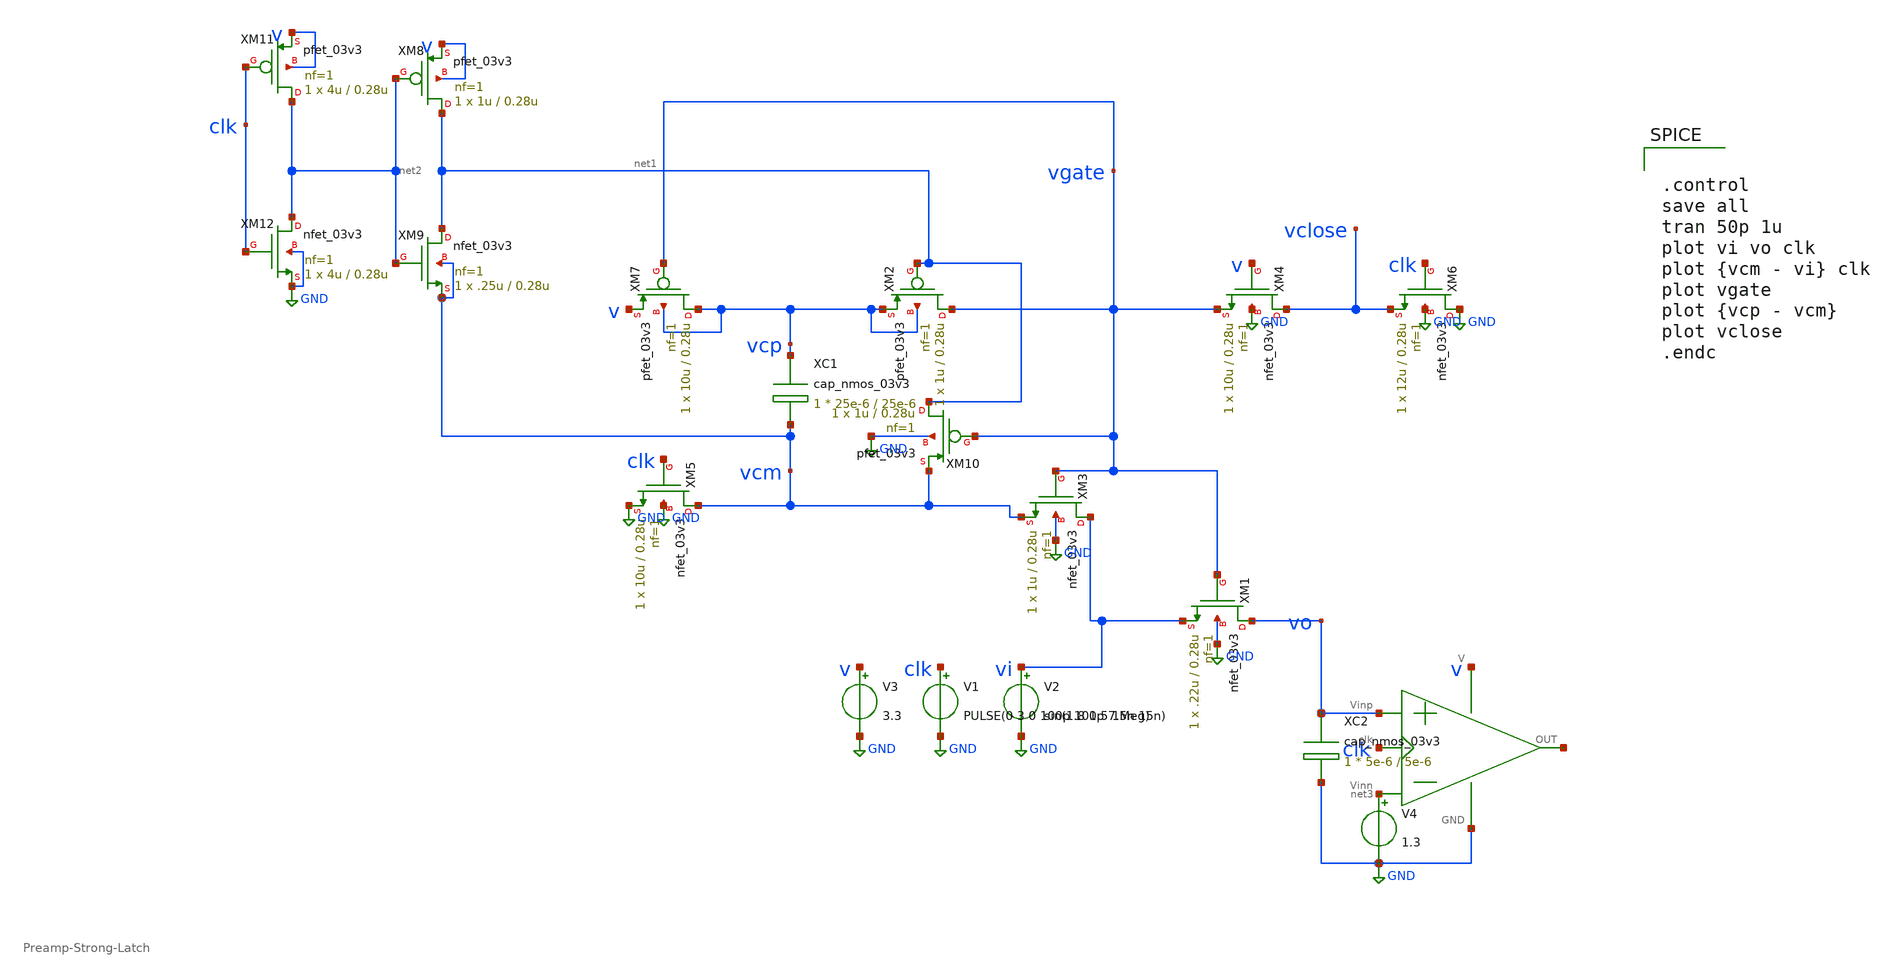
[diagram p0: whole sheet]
** sch_path: btsw/btsw_3.sch
**.subckt btsw_3
XM1 vo vgate vi GND nfet_03v3 L=0.28u W=.22u nf=1 ad='int((nf+1)/2) * W/nf * 0.18u' as='int((nf+2)/2) * W/nf * 0.18u'
+ pd='2*int((nf+1)/2) * (W/nf + 0.18u)' ps='2*int((nf+2)/2) * (W/nf + 0.18u)' nrd='0.18u / W' nrs='0.18u / W'
+ sa=0 sb=0 sd=0 m=1
XM2 vgate net1 vcp vcp pfet_03v3 L=0.28u W=1u nf=1 ad='int((nf+1)/2) * W/nf * 0.18u' as='int((nf+2)/2) * W/nf * 0.18u'
+ pd='2*int((nf+1)/2) * (W/nf + 0.18u)' ps='2*int((nf+2)/2) * (W/nf + 0.18u)' nrd='0.18u / W' nrs='0.18u / W'
+ sa=0 sb=0 sd=0 m=1
XM3 vi vgate vcm GND nfet_03v3 L=0.28u W=1u nf=1 ad='int((nf+1)/2) * W/nf * 0.18u' as='int((nf+2)/2) * W/nf * 0.18u'
+ pd='2*int((nf+1)/2) * (W/nf + 0.18u)' ps='2*int((nf+2)/2) * (W/nf + 0.18u)' nrd='0.18u / W' nrs='0.18u / W'
+ sa=0 sb=0 sd=0 m=1
XM4 vclose v vgate GND nfet_03v3 L=0.28u W=10u nf=1 ad='int((nf+1)/2) * W/nf * 0.18u' as='int((nf+2)/2) * W/nf * 0.18u'
+ pd='2*int((nf+1)/2) * (W/nf + 0.18u)' ps='2*int((nf+2)/2) * (W/nf + 0.18u)' nrd='0.18u / W' nrs='0.18u / W'
+ sa=0 sb=0 sd=0 m=1
XM5 vcm clk GND GND nfet_03v3 L=0.28u W=10u nf=1 ad='int((nf+1)/2) * W/nf * 0.18u' as='int((nf+2)/2) * W/nf * 0.18u'
+ pd='2*int((nf+1)/2) * (W/nf + 0.18u)' ps='2*int((nf+2)/2) * (W/nf + 0.18u)' nrd='0.18u / W' nrs='0.18u / W'
+ sa=0 sb=0 sd=0 m=1
XM6 GND clk vclose GND nfet_03v3 L=0.28u W=12u nf=1 ad='int((nf+1)/2) * W/nf * 0.18u' as='int((nf+2)/2) * W/nf * 0.18u'
+ pd='2*int((nf+1)/2) * (W/nf + 0.18u)' ps='2*int((nf+2)/2) * (W/nf + 0.18u)' nrd='0.18u / W' nrs='0.18u / W'
+ sa=0 sb=0 sd=0 m=1
XM7 vcp vgate v vcp pfet_03v3 L=0.28u W=10u nf=1 ad='int((nf+1)/2) * W/nf * 0.18u' as='int((nf+2)/2) * W/nf * 0.18u'
+ pd='2*int((nf+1)/2) * (W/nf + 0.18u)' ps='2*int((nf+2)/2) * (W/nf + 0.18u)' nrd='0.18u / W' nrs='0.18u / W'
+ sa=0 sb=0 sd=0 m=1
V1 clk GND PULSE(0 3 0 100p 100p 7.5n 15n)
V2 vi GND sin(1.8 1.5 1Meg)
V3 v GND 3.3
XM8 net1 net2 v v pfet_03v3 L=0.28u W=1u nf=1 ad='int((nf+1)/2) * W/nf * 0.18u' as='int((nf+2)/2) * W/nf * 0.18u'
+ pd='2*int((nf+1)/2) * (W/nf + 0.18u)' ps='2*int((nf+2)/2) * (W/nf + 0.18u)' nrd='0.18u / W' nrs='0.18u / W'
+ sa=0 sb=0 sd=0 m=1
XM9 net1 net2 vcm vcm nfet_03v3 L=0.28u W=.25u nf=1 ad='int((nf+1)/2) * W/nf * 0.18u' as='int((nf+2)/2) * W/nf * 0.18u'
+ pd='2*int((nf+1)/2) * (W/nf + 0.18u)' ps='2*int((nf+2)/2) * (W/nf + 0.18u)' nrd='0.18u / W' nrs='0.18u / W'
+ sa=0 sb=0 sd=0 m=1
XM10 net1 vgate vcm GND pfet_03v3 L=0.28u W=1u nf=1 ad='int((nf+1)/2) * W/nf * 0.18u' as='int((nf+2)/2) * W/nf * 0.18u'
+ pd='2*int((nf+1)/2) * (W/nf + 0.18u)' ps='2*int((nf+2)/2) * (W/nf + 0.18u)' nrd='0.18u / W' nrs='0.18u / W'
+ sa=0 sb=0 sd=0 m=1
XM11 net2 clk v v pfet_03v3 L=0.28u W=4u nf=1 ad='int((nf+1)/2) * W/nf * 0.18u' as='int((nf+2)/2) * W/nf * 0.18u'
+ pd='2*int((nf+1)/2) * (W/nf + 0.18u)' ps='2*int((nf+2)/2) * (W/nf + 0.18u)' nrd='0.18u / W' nrs='0.18u / W'
+ sa=0 sb=0 sd=0 m=1
XM12 net2 clk GND GND nfet_03v3 L=0.28u W=4u nf=1 ad='int((nf+1)/2) * W/nf * 0.18u' as='int((nf+2)/2) * W/nf * 0.18u'
+ pd='2*int((nf+1)/2) * (W/nf + 0.18u)' ps='2*int((nf+2)/2) * (W/nf + 0.18u)' nrd='0.18u / W' nrs='0.18u / W'
+ sa=0 sb=0 sd=0 m=1
XC1 vcp vcm cap_nmos_03v3 c_width=25e-6 c_length=25e-6 m=1
X1 v GND vo net3 net4 clk Preamp-Strong-Latch
V4 net3 GND 1.3
XC2 vo GND cap_nmos_03v3 c_width=5e-6 c_length=5e-6 m=1
**** begin user architecture code


.control
save all
tran 50p 1u
plot vi vo clk
plot {vcm - vi} clk
plot vgate
plot {vcp - vcm}
plot vclose
.endc


.include /foss/pdks/gf180mcuC/libs.tech/ngspice/design.ngspice
.lib /foss/pdks/gf180mcuC/libs.tech/ngspice/sm141064.ngspice typical
.lib /foss/pdks/gf180mcuC/libs.tech/ngspice/sm141064.ngspice mimcap_typical
.lib /foss/pdks/gf180mcuC/libs.tech/ngspice/sm141064.ngspice moscap_typical


**** end user architecture code
**.ends
.GLOBAL GND
.end
